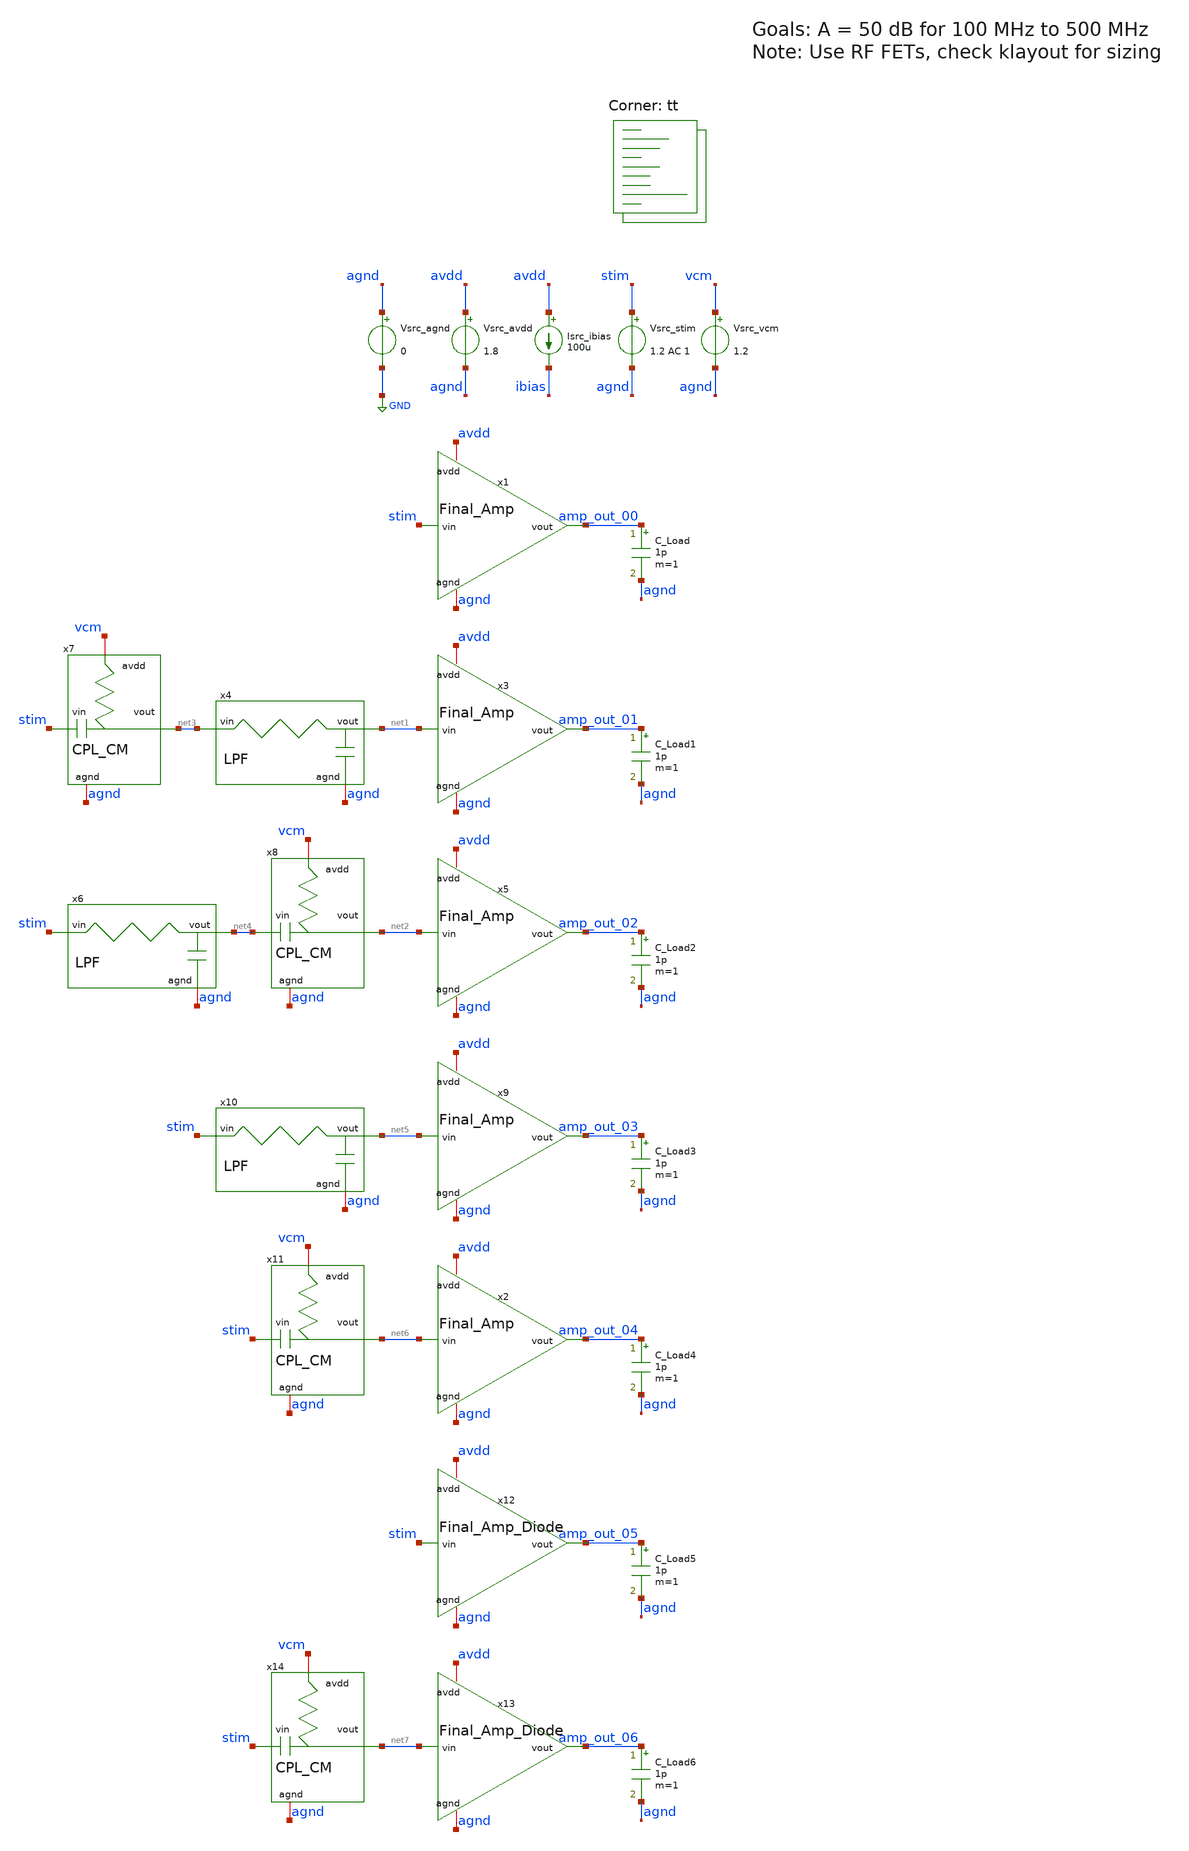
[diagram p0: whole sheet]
** sch_path: AMP/TB_Final_Amp.sch
**.subckt TB_Final_Amp
x1 amp_out_00 stim agnd avdd Final_Amp
Vsrc_agnd agnd GND 0
Vsrc_avdd avdd agnd 1.8
Vsrc_stim stim agnd 1.2 AC 1
Isrc_ibias avdd ibias 100u
C_Load amp_out_00 agnd 1p m=1
x3 amp_out_01 net1 agnd avdd Final_Amp
C_Load1 amp_out_01 agnd 1p m=1
x4 net3 net1 agnd LPF
x5 amp_out_02 net2 agnd avdd Final_Amp
C_Load2 amp_out_02 agnd 1p m=1
x6 stim net4 agnd LPF
x7 vcm agnd net3 stim CPL_CM
x8 vcm agnd net2 net4 CPL_CM
x9 amp_out_03 net5 agnd avdd Final_Amp
C_Load3 amp_out_03 agnd 1p m=1
x10 stim net5 agnd LPF
x2 amp_out_04 net6 agnd avdd Final_Amp
C_Load4 amp_out_04 agnd 1p m=1
x11 vcm agnd net6 stim CPL_CM
C_Load5 amp_out_05 agnd 1p m=1
x12 amp_out_05 stim agnd avdd Final_Amp_Diode
C_Load6 amp_out_06 agnd 1p m=1
x14 vcm agnd net7 stim CPL_CM
x13 amp_out_06 net7 agnd avdd Final_Amp_Diode
Vsrc_vcm vcm agnd 1.2
**** begin user architecture code

* this option enables mos model bin
* selection based on W/NF instead of W

.option savecurrents

.control
save all
op


* Print newline
echo

* Print stats for each MOSFET
* xm1 xm2 xm3 xm4
foreach amp x1 x3 x5 x9 x2
 foreach mos xm1
  * Save stats
  save @m.{$amp}.{$mos}.msky130_fd_pr__nfet_01v8[gm]
  let vth   = @m.{$amp}.{$mos}.msky130_fd_pr__nfet_01v8[vth]
  let vdsat = @m.{$amp}.{$mos}.msky130_fd_pr__nfet_01v8[vdsat]
  let gm    = @m.{$amp}.{$mos}.msky130_fd_pr__nfet_01v8[gm]
  let gds   = @m.{$amp}.{$mos}.msky130_fd_pr__nfet_01v8[gds]

  * Print stats
  echo Stats for $amp $mos:
  print vth
  print vdsat
  print gm
  print gds

  * Print newline
  echo

 end
end

foreach amp x12 x13
 foreach mos xm1 xm2
  * Save stats
  save @m.{$amp}.{$mos}.msky130_fd_pr__nfet_01v8[gm]
  let vth   = @m.{$amp}.{$mos}.msky130_fd_pr__nfet_01v8[vth]
  let vdsat = @m.{$amp}.{$mos}.msky130_fd_pr__nfet_01v8[vdsat]
  let gm    = @m.{$amp}.{$mos}.msky130_fd_pr__nfet_01v8[gm]
  let gds   = @m.{$amp}.{$mos}.msky130_fd_pr__nfet_01v8[gds]

  * Print stats
  echo Stats for $amp $mos:
  print vth
  print vdsat
  print gm
  print gds

  * Print newline
  echo

 end
end

* Print region of operation
echo Regions of Operation:
foreach amp x1 x3 x5 x9 x2
 foreach nmos xm1
  * Save stats
  let vds = @m.{$amp}.{$nmos}.msky130_fd_pr__nfet_01v8[vds]
  let vgs = @m.{$amp}.{$nmos}.msky130_fd_pr__nfet_01v8[vgs]
  let vth = @m.{$amp}.{$nmos}.msky130_fd_pr__nfet_01v8[vth]

  * Check and print regions
  if (vgs <= vth)
   echo $amp $nmos: N Cutoff
   print vgs
   print vth
  end
  if (vgs > vth) & (vds <= (vgs - vth))
   echo $amp $nmos: N Triode
   print vgs
   print vth
   print vds
  end
  if (vgs > vth) & (vds > (vgs - vth))
   echo $amp $nmos: N Saturation
  end
 end
end

foreach amp x12 x13
 foreach nmos xm1 xm2
  * Save stats
  let vds = @m.{$amp}.{$nmos}.msky130_fd_pr__nfet_01v8[vds]
  let vgs = @m.{$amp}.{$nmos}.msky130_fd_pr__nfet_01v8[vgs]
  let vth = @m.{$amp}.{$nmos}.msky130_fd_pr__nfet_01v8[vth]

  * Check and print regions
  if (vgs <= vth)
   echo $amp $nmos: N Cutoff
   print vgs
   print vth
  end
  if (vgs > vth) & (vds <= (vgs - vth))
   echo $amp $nmos: N Triode
   print vgs
   print vth
   print vds
  end
  if (vgs > vth) & (vds > (vgs - vth))
   echo $amp $nmos: N Saturation
  end
 end
end

* Print newline
echo

* Sweep frequency
write TB_Final_Amp.raw
set appendwrite
ac dec 100 1 1e11
remzerovec

* Calculate gain
let ratio_00 = v(amp_out_00)/v(stim)
let ratio_01 = v(amp_out_01)/v(stim)
let ratio_02 = v(amp_out_02)/v(stim)
let ratio_03 = v(amp_out_03)/v(stim)
let ratio_04 = v(amp_out_04)/v(stim)
let ratio_05 = v(amp_out_05)/v(stim)
let ratio_06 = v(amp_out_06)/v(stim)

let gain_00 = db(mag(ratio_00))
let gain_01 = db(mag(ratio_01))
let gain_02 = db(mag(ratio_02))
let gain_03 = db(mag(ratio_03))
let gain_04 = db(mag(ratio_04))
let gain_05 = db(mag(ratio_05))
let gain_06 = db(mag(ratio_06))

write TB_Final_Amp.raw

.endc


.lib $::SKYWATER_MODELS/sky130.lib.spice tt
**** end user architecture code
**.ends
.GLOBAL GND
.end
